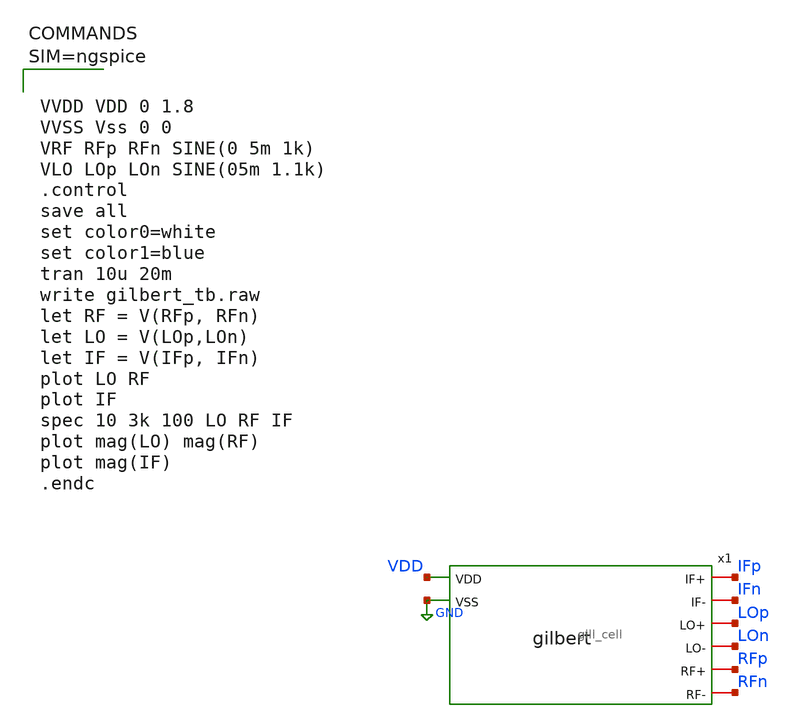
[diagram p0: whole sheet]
** sch_path: hw03/xschem/gilbert_tb.sch
**.subckt gilbert_tb
x1 VDD IFp IFn LOp LOn RFp RFn GND gill_cell
**** begin user architecture code

** opencircuitdesign pdks install
.lib $::SKYWATER_MODELS/sky130.lib.spice tt





VVDD VDD 0 1.8
VVSS Vss 0 0
VRF RFp RFn SINE(0 5m 1k)
VLO LOp LOn SINE(05m 1.1k)
.control
save all
set color0=white
set color1=blue
tran 10u 20m
write gilbert_tb.raw
let RF = V(RFp, RFn)
let LO = V(LOp,LOn)
let IF = V(IFp, IFn)
plot LO RF
plot IF
spec 10 3k 100 LO RF IF
plot mag(LO) mag(RF)
plot mag(IF)
.endc



**** end user architecture code
**.ends

* expanding   symbol:  gill_cell.sym # of pins=8
** sym_path: hw03/xschem/gill_cell.sym
** sch_path: hw03/xschem/gill_cell.sch
.subckt gill_cell VDD IF+ IF- LO+ LO- RF+ RF- VSS
*.ipin VSS
*.ipin VDD
*.iopin IF+
*.iopin IF-
*.iopin LO+
*.iopin LO-
*.iopin RF+
*.iopin RF-
XM1 net1 net1 VSS VSS sky130_fd_pr__nfet_01v8_lvt L=0.15 W=1 nf=1 ad='int((1 + 1)/2) * 1 / 1 * 0.29'
+ as='int((1 + 2)/2) * 1 / 1 * 0.29' pd='2*int((1 + 1)/2) * (1 / 1 + 0.29)' ps='2*int((1 + 2)/2) * (1 / 1 + 0.29)'
+ nrd='0.29 / 1 ' nrs='0.29 / 1 ' sa=0 sb=0 sd=0 mult=1 m=1
XM2 net2 net1 VSS VSS sky130_fd_pr__nfet_01v8_lvt L=0.15 W=1 nf=1 ad='int((1 + 1)/2) * 1 / 1 * 0.29'
+ as='int((1 + 2)/2) * 1 / 1 * 0.29' pd='2*int((1 + 1)/2) * (1 / 1 + 0.29)' ps='2*int((1 + 2)/2) * (1 / 1 + 0.29)'
+ nrd='0.29 / 1 ' nrs='0.29 / 1 ' sa=0 sb=0 sd=0 mult=1 m=1
I_in net6 net1 0
.save i(i_in)
I_out net2 net3 0
.save i(i_out)
XM3 net4 RF+ net3 VSS sky130_fd_pr__nfet_01v8_lvt L=0.15 W=1 nf=1 ad='int((1 + 1)/2) * 1 / 1 * 0.29'
+ as='int((1 + 2)/2) * 1 / 1 * 0.29' pd='2*int((1 + 1)/2) * (1 / 1 + 0.29)' ps='2*int((1 + 2)/2) * (1 / 1 + 0.29)'
+ nrd='0.29 / 1 ' nrs='0.29 / 1 ' sa=0 sb=0 sd=0 mult=1 m=1
XM4 net5 RF- net3 VSS sky130_fd_pr__nfet_01v8_lvt L=0.15 W=1 nf=1 ad='int((1 + 1)/2) * 1 / 1 * 0.29'
+ as='int((1 + 2)/2) * 1 / 1 * 0.29' pd='2*int((1 + 1)/2) * (1 / 1 + 0.29)' ps='2*int((1 + 2)/2) * (1 / 1 + 0.29)'
+ nrd='0.29 / 1 ' nrs='0.29 / 1 ' sa=0 sb=0 sd=0 mult=1 m=1
XM5 IF+ LO+ net4 VSS sky130_fd_pr__nfet_01v8_lvt L=0.15 W=1 nf=1 ad='int((1 + 1)/2) * 1 / 1 * 0.29' as='int((1 + 2)/2) * 1 / 1 * 0.29'
+ pd='2*int((1 + 1)/2) * (1 / 1 + 0.29)' ps='2*int((1 + 2)/2) * (1 / 1 + 0.29)' nrd='0.29 / 1 ' nrs='0.29 / 1 '
+ sa=0 sb=0 sd=0 mult=1 m=1
XM6 IF- LO- net4 VSS sky130_fd_pr__nfet_01v8_lvt L=0.15 W=1 nf=1 ad='int((1 + 1)/2) * 1 / 1 * 0.29' as='int((1 + 2)/2) * 1 / 1 * 0.29'
+ pd='2*int((1 + 1)/2) * (1 / 1 + 0.29)' ps='2*int((1 + 2)/2) * (1 / 1 + 0.29)' nrd='0.29 / 1 ' nrs='0.29 / 1 '
+ sa=0 sb=0 sd=0 mult=1 m=1
XM7 IF+ LO- net5 VSS sky130_fd_pr__nfet_01v8_lvt L=0.15 W=1 nf=1 ad='int((1 + 1)/2) * 1 / 1 * 0.29' as='int((1 + 2)/2) * 1 / 1 * 0.29'
+ pd='2*int((1 + 1)/2) * (1 / 1 + 0.29)' ps='2*int((1 + 2)/2) * (1 / 1 + 0.29)' nrd='0.29 / 1 ' nrs='0.29 / 1 '
+ sa=0 sb=0 sd=0 mult=1 m=1
XM8 IF- LO+ net5 VSS sky130_fd_pr__nfet_01v8_lvt L=0.15 W=1 nf=1 ad='int((1 + 1)/2) * 1 / 1 * 0.29' as='int((1 + 2)/2) * 1 / 1 * 0.29'
+ pd='2*int((1 + 1)/2) * (1 / 1 + 0.29)' ps='2*int((1 + 2)/2) * (1 / 1 + 0.29)' nrd='0.29 / 1 ' nrs='0.29 / 1 '
+ sa=0 sb=0 sd=0 mult=1 m=1
XR1 IF+ VDD VDD sky130_fd_pr__res_xhigh_po_0p69 L=0.69*20 mult=1 m=1
XR3 IF- VDD VDD sky130_fd_pr__res_xhigh_po_0p69 L=0.69*20 mult=1 m=1
XR2 net6 VDD VDD sky130_fd_pr__res_xhigh_po_0p69 L=0.69*9 mult=1 m=1
.ends

.GLOBAL GND
.end
